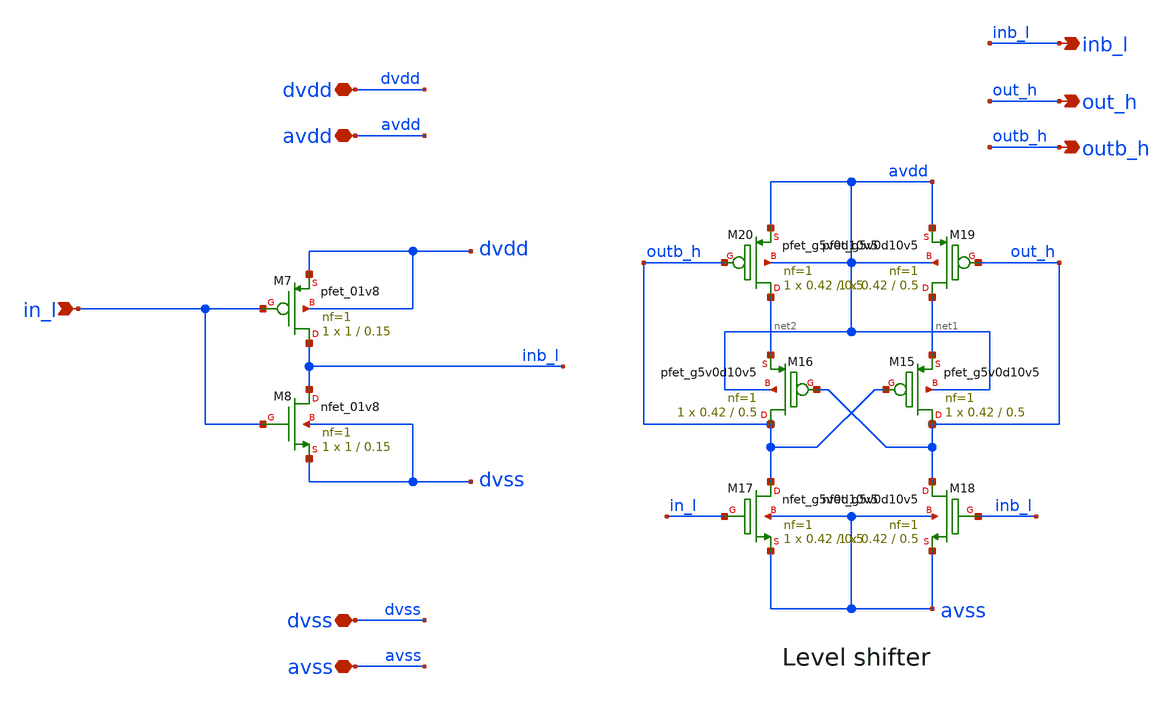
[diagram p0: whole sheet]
** sch_path: xschem/level_shifter.sch
**.subckt level_shifter in_l dvdd avdd dvss avss out_h outb_h inb_l
*.ipin in_l
*.iopin dvdd
*.iopin avdd
*.iopin dvss
*.iopin avss
*.opin out_h
*.opin outb_h
*.opin inb_l
XM7 inb_l in_l dvdd dvdd sky130_fd_pr__pfet_01v8 L=0.15 W=1 nf=1 ad='int((nf+1)/2) * W/nf * 0.29' as='int((nf+2)/2) * W/nf * 0.29'
+ pd='2*int((nf+1)/2) * (W/nf + 0.29)' ps='2*int((nf+2)/2) * (W/nf + 0.29)' nrd='0.29 / W' nrs='0.29 / W'
+ sa=0 sb=0 sd=0 mult=1 m=1
XM8 inb_l in_l dvss dvss sky130_fd_pr__nfet_01v8 L=0.15 W=1 nf=1 ad='int((nf+1)/2) * W/nf * 0.29' as='int((nf+2)/2) * W/nf * 0.29'
+ pd='2*int((nf+1)/2) * (W/nf + 0.29)' ps='2*int((nf+2)/2) * (W/nf + 0.29)' nrd='0.29 / W' nrs='0.29 / W'
+ sa=0 sb=0 sd=0 mult=1 m=1
XM15 out_h outb_h net1 avdd sky130_fd_pr__pfet_g5v0d10v5 L=0.5 W=0.42 nf=1 ad='int((nf+1)/2) * W/nf * 0.29'
+ as='int((nf+2)/2) * W/nf * 0.29' pd='2*int((nf+1)/2) * (W/nf + 0.29)' ps='2*int((nf+2)/2) * (W/nf + 0.29)'
+ nrd='0.29 / W' nrs='0.29 / W' sa=0 sb=0 sd=0 mult=1 m=1
XM16 outb_h out_h net2 avdd sky130_fd_pr__pfet_g5v0d10v5 L=0.5 W=0.42 nf=1 ad='int((nf+1)/2) * W/nf * 0.29'
+ as='int((nf+2)/2) * W/nf * 0.29' pd='2*int((nf+1)/2) * (W/nf + 0.29)' ps='2*int((nf+2)/2) * (W/nf + 0.29)'
+ nrd='0.29 / W' nrs='0.29 / W' sa=0 sb=0 sd=0 mult=1 m=1
XM17 outb_h in_l avss avss sky130_fd_pr__nfet_g5v0d10v5 L=0.5 W=0.42 nf=1 ad='int((nf+1)/2) * W/nf * 0.29'
+ as='int((nf+2)/2) * W/nf * 0.29' pd='2*int((nf+1)/2) * (W/nf + 0.29)' ps='2*int((nf+2)/2) * (W/nf + 0.29)'
+ nrd='0.29 / W' nrs='0.29 / W' sa=0 sb=0 sd=0 mult=1 m=1
XM18 out_h inb_l avss avss sky130_fd_pr__nfet_g5v0d10v5 L=0.5 W=0.42 nf=1 ad='int((nf+1)/2) * W/nf * 0.29'
+ as='int((nf+2)/2) * W/nf * 0.29' pd='2*int((nf+1)/2) * (W/nf + 0.29)' ps='2*int((nf+2)/2) * (W/nf + 0.29)'
+ nrd='0.29 / W' nrs='0.29 / W' sa=0 sb=0 sd=0 mult=1 m=1
XM19 net1 out_h avdd avdd sky130_fd_pr__pfet_g5v0d10v5 L=0.5 W=0.42 nf=1 ad='int((nf+1)/2) * W/nf * 0.29'
+ as='int((nf+2)/2) * W/nf * 0.29' pd='2*int((nf+1)/2) * (W/nf + 0.29)' ps='2*int((nf+2)/2) * (W/nf + 0.29)'
+ nrd='0.29 / W' nrs='0.29 / W' sa=0 sb=0 sd=0 mult=1 m=1
XM20 net2 outb_h avdd avdd sky130_fd_pr__pfet_g5v0d10v5 L=0.5 W=0.42 nf=1 ad='int((nf+1)/2) * W/nf * 0.29'
+ as='int((nf+2)/2) * W/nf * 0.29' pd='2*int((nf+1)/2) * (W/nf + 0.29)' ps='2*int((nf+2)/2) * (W/nf + 0.29)'
+ nrd='0.29 / W' nrs='0.29 / W' sa=0 sb=0 sd=0 mult=1 m=1
**.ends
.end
